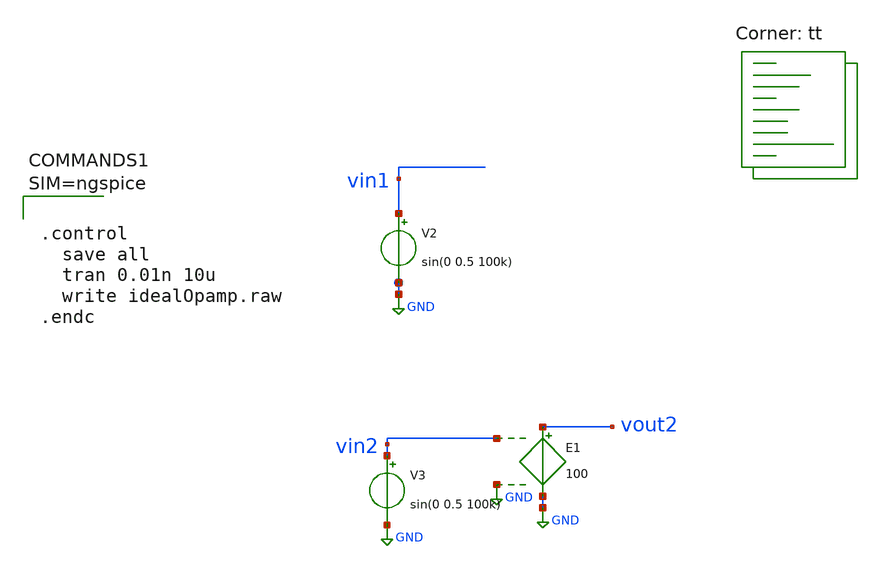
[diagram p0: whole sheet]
** sch_path: custom_gds/tt_um_bgr_agolmanesh/xschem/idealOpamp.sch
**.subckt idealOpamp
E1 vout2 GND vin2 GND 100
V2 vin1 GND sin(0 0.5 100k)
V3 vin2 GND sin(0 0.5 100k)
**** begin user architecture code



.control
  save all
  tran 0.01n 10u
  write idealOpamp.raw
.endc



.lib $::SKYWATER_MODELS/sky130.lib.spice tt
**** end user architecture code
**.ends
.GLOBAL GND
.end
